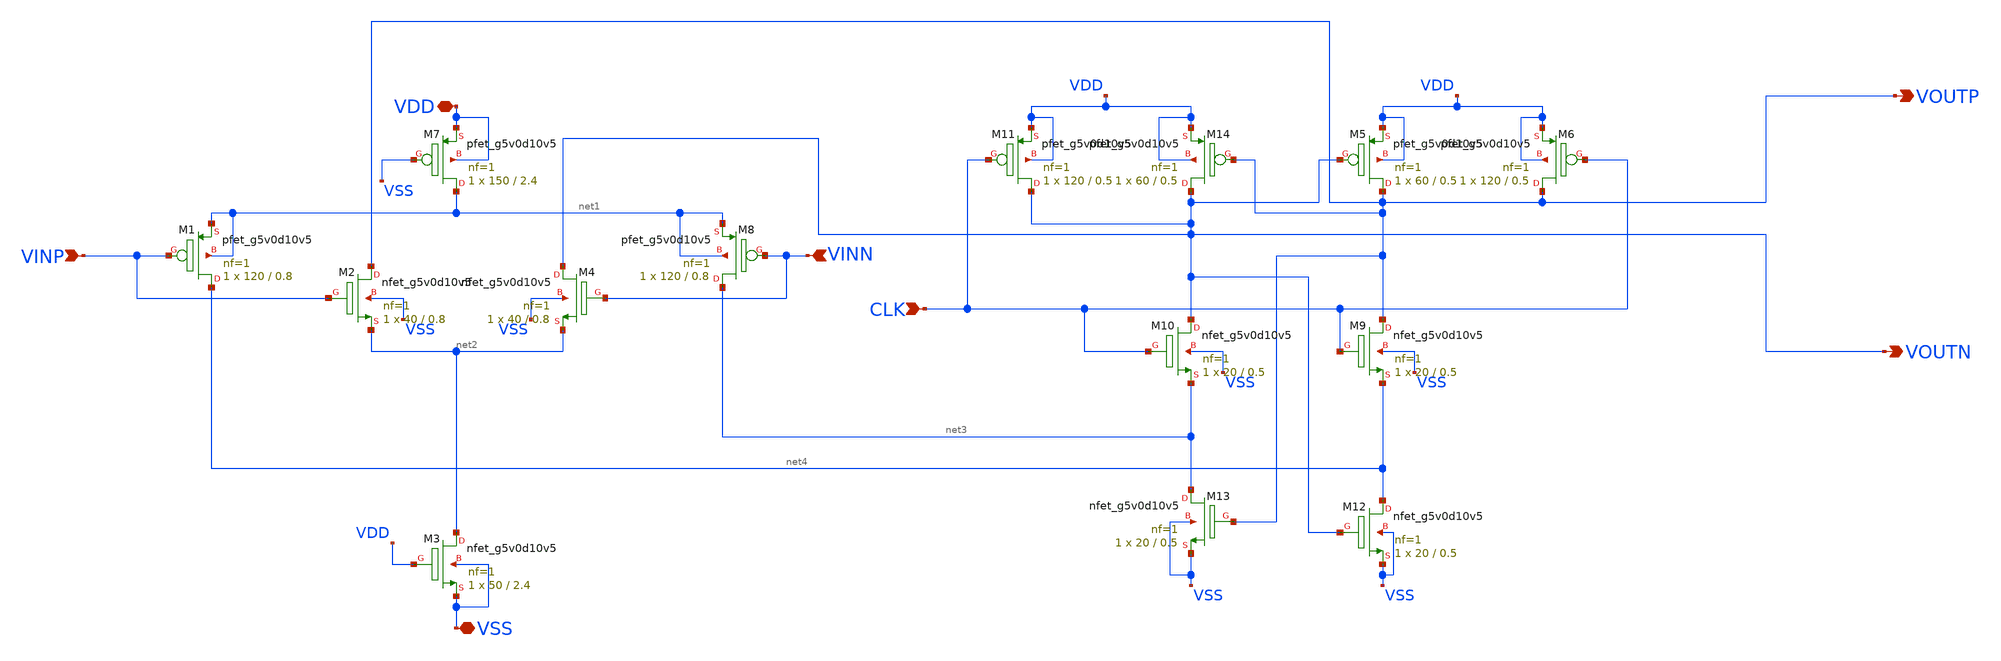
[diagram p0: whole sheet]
** sch_path: xschem/comp.sch
**.subckt comp VOUTP VOUTN VINP VINN CLK VDD VSS
*.opin VOUTP
*.opin VOUTN
*.ipin VINP
*.ipin VINN
*.ipin CLK
*.iopin VDD
*.iopin VSS
XM8 net3 VINN net1 net1 sky130_fd_pr__pfet_g5v0d10v5 L=0.8 W=120 nf=1 ad='int((1 + 1)/2) * 120 / 1 * 0.29'
+ as='int((1 + 2)/2) * 120 / 1 * 0.29' pd='2*int((1 + 1)/2) * (120 / 1 + 0.29)' ps='2*int((1 + 2)/2) * (120 / 1 + 0.29)'
+ nrd='0.29 / 120 ' nrs='0.29 / 120 ' sa=0 sb=0 sd=0 mult=1 m=1
XM7 net1 VSS VDD VDD sky130_fd_pr__pfet_g5v0d10v5 L=2.4 W=150 nf=1 ad='int((1 + 1)/2) * 150 / 1 * 0.29'
+ as='int((1 + 2)/2) * 150 / 1 * 0.29' pd='2*int((1 + 1)/2) * (150 / 1 + 0.29)' ps='2*int((1 + 2)/2) * (150 / 1 + 0.29)'
+ nrd='0.29 / 150 ' nrs='0.29 / 150 ' sa=0 sb=0 sd=0 mult=1 m=1
XM1 net4 VINP net1 net1 sky130_fd_pr__pfet_g5v0d10v5 L=0.8 W=120 nf=1 ad='int((1 + 1)/2) * 120 / 1 * 0.29'
+ as='int((1 + 2)/2) * 120 / 1 * 0.29' pd='2*int((1 + 1)/2) * (120 / 1 + 0.29)' ps='2*int((1 + 2)/2) * (120 / 1 + 0.29)'
+ nrd='0.29 / 120 ' nrs='0.29 / 120 ' sa=0 sb=0 sd=0 mult=1 m=1
XM2 VOUTP VINP net2 VSS sky130_fd_pr__nfet_g5v0d10v5 L=0.8 W=40 nf=1 ad='int((1 + 1)/2) * 40 / 1 * 0.29'
+ as='int((1 + 2)/2) * 40 / 1 * 0.29' pd='2*int((1 + 1)/2) * (40 / 1 + 0.29)' ps='2*int((1 + 2)/2) * (40 / 1 + 0.29)'
+ nrd='0.29 / 40 ' nrs='0.29 / 40 ' sa=0 sb=0 sd=0 mult=1 m=1
XM3 net2 VDD VSS VSS sky130_fd_pr__nfet_g5v0d10v5 L=2.4 W=50 nf=1 ad='int((1 + 1)/2) * 50 / 1 * 0.29'
+ as='int((1 + 2)/2) * 50 / 1 * 0.29' pd='2*int((1 + 1)/2) * (50 / 1 + 0.29)' ps='2*int((1 + 2)/2) * (50 / 1 + 0.29)'
+ nrd='0.29 / 50 ' nrs='0.29 / 50 ' sa=0 sb=0 sd=0 mult=1 m=1
XM4 VOUTN VINN net2 VSS sky130_fd_pr__nfet_g5v0d10v5 L=0.8 W=40 nf=1 ad='int((1 + 1)/2) * 40 / 1 * 0.29'
+ as='int((1 + 2)/2) * 40 / 1 * 0.29' pd='2*int((1 + 1)/2) * (40 / 1 + 0.29)' ps='2*int((1 + 2)/2) * (40 / 1 + 0.29)'
+ nrd='0.29 / 40 ' nrs='0.29 / 40 ' sa=0 sb=0 sd=0 mult=1 m=1
XM9 VOUTP CLK net4 VSS sky130_fd_pr__nfet_g5v0d10v5 L=0.5 W=20 nf=1 ad='int((1 + 1)/2) * 20 / 1 * 0.29'
+ as='int((1 + 2)/2) * 20 / 1 * 0.29' pd='2*int((1 + 1)/2) * (20 / 1 + 0.29)' ps='2*int((1 + 2)/2) * (20 / 1 + 0.29)'
+ nrd='0.29 / 20 ' nrs='0.29 / 20 ' sa=0 sb=0 sd=0 mult=1 m=1
XM10 VOUTN CLK net3 VSS sky130_fd_pr__nfet_g5v0d10v5 L=0.5 W=20 nf=1 ad='int((1 + 1)/2) * 20 / 1 * 0.29'
+ as='int((1 + 2)/2) * 20 / 1 * 0.29' pd='2*int((1 + 1)/2) * (20 / 1 + 0.29)' ps='2*int((1 + 2)/2) * (20 / 1 + 0.29)'
+ nrd='0.29 / 20 ' nrs='0.29 / 20 ' sa=0 sb=0 sd=0 mult=1 m=1
XM12 net4 VOUTN VSS VSS sky130_fd_pr__nfet_g5v0d10v5 L=0.5 W=20 nf=1 ad='int((1 + 1)/2) * 20 / 1 * 0.29'
+ as='int((1 + 2)/2) * 20 / 1 * 0.29' pd='2*int((1 + 1)/2) * (20 / 1 + 0.29)' ps='2*int((1 + 2)/2) * (20 / 1 + 0.29)'
+ nrd='0.29 / 20 ' nrs='0.29 / 20 ' sa=0 sb=0 sd=0 mult=1 m=1
XM13 net3 VOUTP VSS VSS sky130_fd_pr__nfet_g5v0d10v5 L=0.5 W=20 nf=1 ad='int((1 + 1)/2) * 20 / 1 * 0.29'
+ as='int((1 + 2)/2) * 20 / 1 * 0.29' pd='2*int((1 + 1)/2) * (20 / 1 + 0.29)' ps='2*int((1 + 2)/2) * (20 / 1 + 0.29)'
+ nrd='0.29 / 20 ' nrs='0.29 / 20 ' sa=0 sb=0 sd=0 mult=1 m=1
XM14 VOUTN VOUTP VDD VDD sky130_fd_pr__pfet_g5v0d10v5 L=0.5 W=60 nf=1 ad='int((1 + 1)/2) * 60 / 1 * 0.29'
+ as='int((1 + 2)/2) * 60 / 1 * 0.29' pd='2*int((1 + 1)/2) * (60 / 1 + 0.29)' ps='2*int((1 + 2)/2) * (60 / 1 + 0.29)'
+ nrd='0.29 / 60 ' nrs='0.29 / 60 ' sa=0 sb=0 sd=0 mult=1 m=1
XM11 VOUTN CLK VDD VDD sky130_fd_pr__pfet_g5v0d10v5 L=0.5 W=120 nf=1 ad='int((1 + 1)/2) * 120 / 1 * 0.29'
+ as='int((1 + 2)/2) * 120 / 1 * 0.29' pd='2*int((1 + 1)/2) * (120 / 1 + 0.29)' ps='2*int((1 + 2)/2) * (120 / 1 + 0.29)'
+ nrd='0.29 / 120 ' nrs='0.29 / 120 ' sa=0 sb=0 sd=0 mult=1 m=1
XM5 VOUTP VOUTN VDD VDD sky130_fd_pr__pfet_g5v0d10v5 L=0.5 W=60 nf=1 ad='int((1 + 1)/2) * 60 / 1 * 0.29'
+ as='int((1 + 2)/2) * 60 / 1 * 0.29' pd='2*int((1 + 1)/2) * (60 / 1 + 0.29)' ps='2*int((1 + 2)/2) * (60 / 1 + 0.29)'
+ nrd='0.29 / 60 ' nrs='0.29 / 60 ' sa=0 sb=0 sd=0 mult=1 m=1
XM6 VOUTP CLK VDD VDD sky130_fd_pr__pfet_g5v0d10v5 L=0.5 W=120 nf=1 ad='int((1 + 1)/2) * 120 / 1 * 0.29'
+ as='int((1 + 2)/2) * 120 / 1 * 0.29' pd='2*int((1 + 1)/2) * (120 / 1 + 0.29)' ps='2*int((1 + 2)/2) * (120 / 1 + 0.29)'
+ nrd='0.29 / 120 ' nrs='0.29 / 120 ' sa=0 sb=0 sd=0 mult=1 m=1
**.ends
.end
